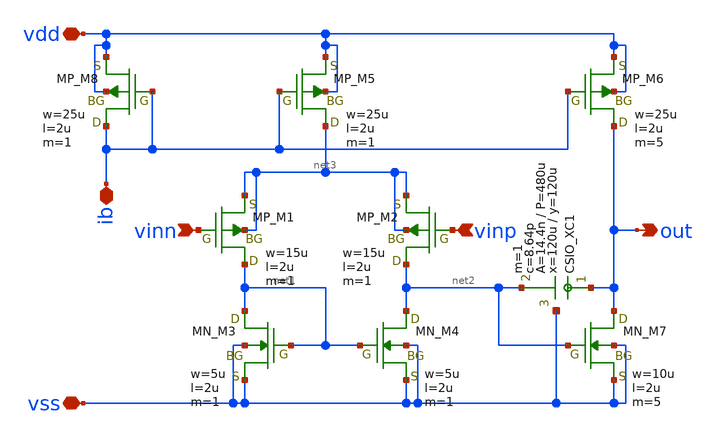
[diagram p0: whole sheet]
** sch_path: member_project/DCDC/ShuntaroOHNO/xschem/opamp_slow.sch
**.subckt opamp_slow vdd vss vinn vinp out ib
*.iopin vdd
*.iopin vss
*.ipin vinn
*.ipin vinp
*.opin out
*.iopin ib
XM1 net1 vinn net3 net3 PMOS w=15u l=2u as=0 ad=0 ps=0 pd=0 nrd=0 nrs=0 m=1
XM2 net2 vinp net3 net3 PMOS w=15u l=2u as=0 ad=0 ps=0 pd=0 nrd=0 nrs=0 m=1
XM3 net1 net1 vss vss NMOS w=5u l=2u as=0 ad=0 ps=0 pd=0 nrd=0 nrs=0 m=1
XM4 net2 net1 vss vss NMOS w=5u l=2u as=0 ad=0 ps=0 pd=0 nrd=0 nrs=0 m=1
XM5 net3 ib vdd vdd PMOS w=25u l=2u as=0 ad=0 ps=0 pd=0 nrd=0 nrs=0 m=1
XM6 out ib vdd vdd PMOS w=25u l=2u as=0 ad=0 ps=0 pd=0 nrd=0 nrs=0 m=5
XM7 out net2 vss vss NMOS w=10u l=2u as=0 ad=0 ps=0 pd=0 nrd=0 nrs=0 m=5
XM8 ib ib vdd vdd PMOS w=25u l=2u as=0 ad=0 ps=0 pd=0 nrd=0 nrs=0 m=1
XXC1 out net2 vss F_CSIO c=8.64p x=120u y=120u m=1
**.ends
.end
